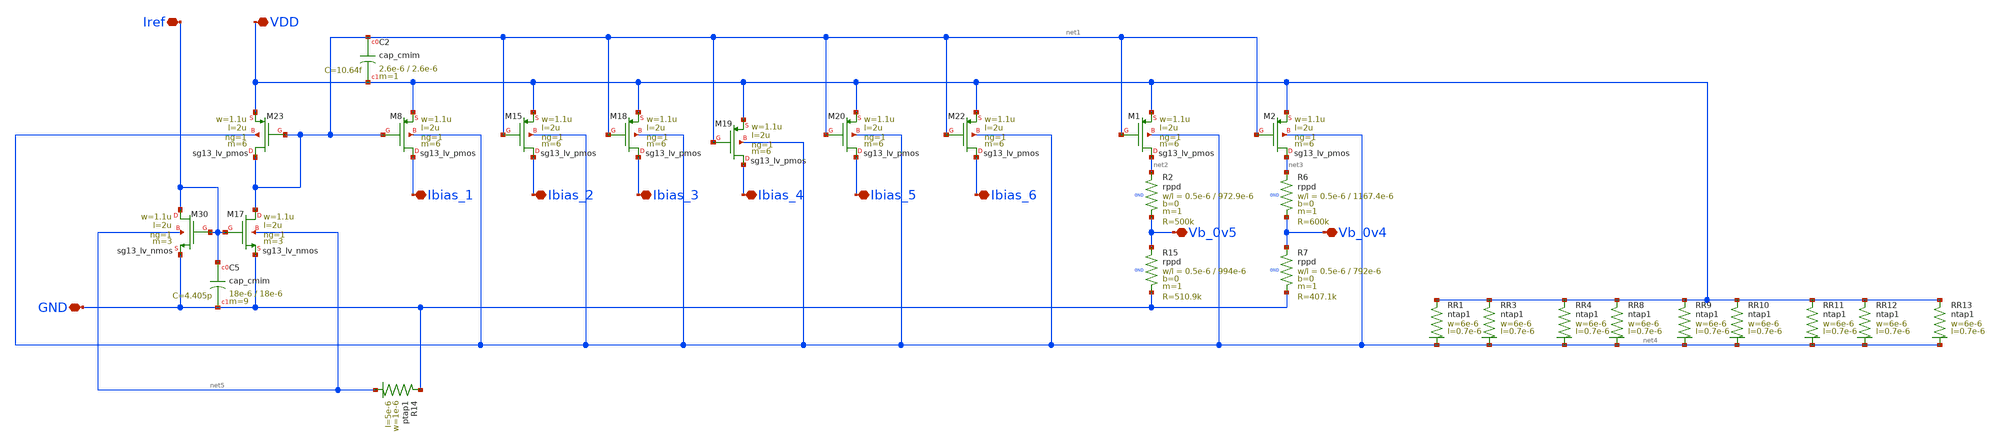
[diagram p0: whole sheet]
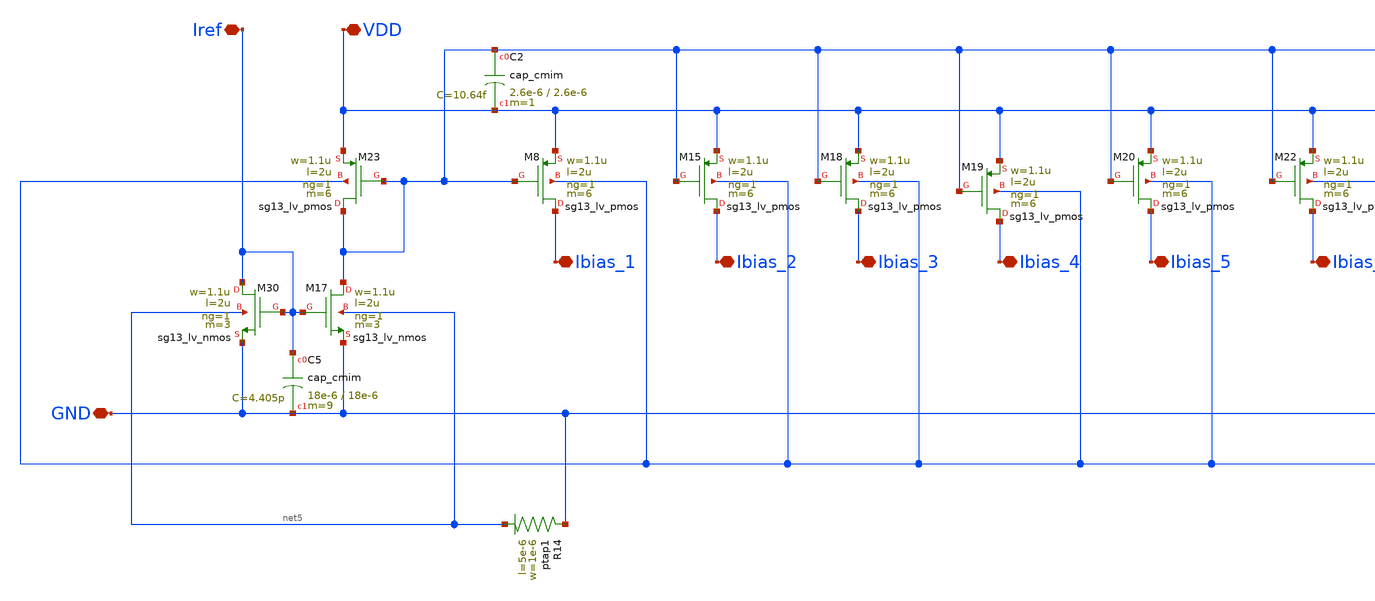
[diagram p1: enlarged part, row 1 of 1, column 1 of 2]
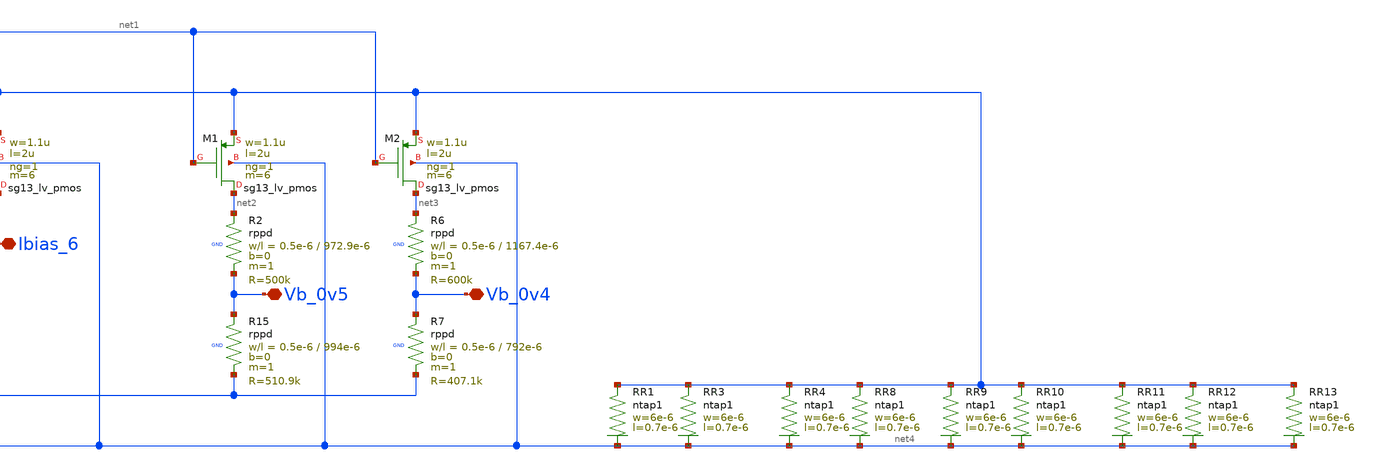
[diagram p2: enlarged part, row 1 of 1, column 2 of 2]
** sch_path: Layouts/ib_ctat_ptat/out_mirror.sch
**.subckt out_mirror Ibias_1 Ibias_2 Ibias_3 Ibias_4 Ibias_5 Ibias_6 Vb_0v4 Vb_0v5 GND VDD Iref
*.iopin Ibias_1
*.iopin Ibias_2
*.iopin Ibias_3
*.iopin Ibias_4
*.iopin Ibias_5
*.iopin Ibias_6
*.iopin Vb_0v4
*.iopin Vb_0v5
*.iopin GND
*.iopin VDD
*.iopin Iref
XM30 Iref Iref GND net5 sg13_lv_nmos w=1.1u l=2u ng=1 m=3 mm_ok=1
XR2 net2 Vb_0v5 GND rppd w=0.5e-6 l=972.9e-6 m=1 b=0 mm_ok=1
XR6 net3 Vb_0v4 GND rppd w=0.5e-6 l=1167.4e-6 m=1 b=0 mm_ok=1
XM17 net1 Iref GND net5 sg13_lv_nmos w=1.1u l=2u ng=1 m=3 mm_ok=1
XM23 net1 net1 VDD net4 sg13_lv_pmos w=1.1u l=2u ng=1 m=6 mm_ok=1
XM8 Ibias_1 net1 VDD net4 sg13_lv_pmos w=1.1u l=2u ng=1 m=6 mm_ok=1
XM15 Ibias_2 net1 VDD net4 sg13_lv_pmos w=1.1u l=2u ng=1 m=6 mm_ok=1
XM18 Ibias_3 net1 VDD net4 sg13_lv_pmos w=1.1u l=2u ng=1 m=6 mm_ok=1
XM19 Ibias_4 net1 VDD net4 sg13_lv_pmos w=1.1u l=2u ng=1 m=6 mm_ok=1
XM20 Ibias_5 net1 VDD net4 sg13_lv_pmos w=1.1u l=2u ng=1 m=6 mm_ok=1
XM22 Ibias_6 net1 VDD net4 sg13_lv_pmos w=1.1u l=2u ng=1 m=6 mm_ok=1
XC5 Iref GND cap_cmim w=18e-6 l=18e-6 m=9 mm_ok=1
XC2 net1 VDD cap_cmim w=2.6e-6 l=2.6e-6 m=1 mm_ok=1
XR1 VDD net4 ntap1 R=55.68 w=6e-6 l=0.7e-6
XR3 VDD net4 ntap1 R=55.68 w=6e-6 l=0.7e-6
XR4 VDD net4 ntap1 R=55.68 w=6e-6 l=0.7e-6
XR8 VDD net4 ntap1 R=55.68 w=6e-6 l=0.7e-6
XR9 VDD net4 ntap1 R=55.68 w=6e-6 l=0.7e-6
XR10 VDD net4 ntap1 R=55.68 w=6e-6 l=0.7e-6
XR11 VDD net4 ntap1 R=55.68 w=6e-6 l=0.7e-6
XR12 VDD net4 ntap1 R=55.68 w=6e-6 l=0.7e-6
XR13 VDD net4 ntap1 R=55.68 w=6e-6 l=0.7e-6
XR14 GND net5 ptap1 R=57.65 w=1e-6 l=5e-6
XM1 net2 net1 VDD net4 sg13_lv_pmos w=1.1u l=2u ng=1 m=6 mm_ok=1
XM2 net3 net1 VDD net4 sg13_lv_pmos w=1.1u l=2u ng=1 m=6 mm_ok=1
XR15 Vb_0v5 GND GND rppd w=0.5e-6 l=994e-6 m=1 b=0 mm_ok=1
XR7 Vb_0v4 GND GND rppd w=0.5e-6 l=792e-6 m=1 b=0 mm_ok=1
**.ends
.end
